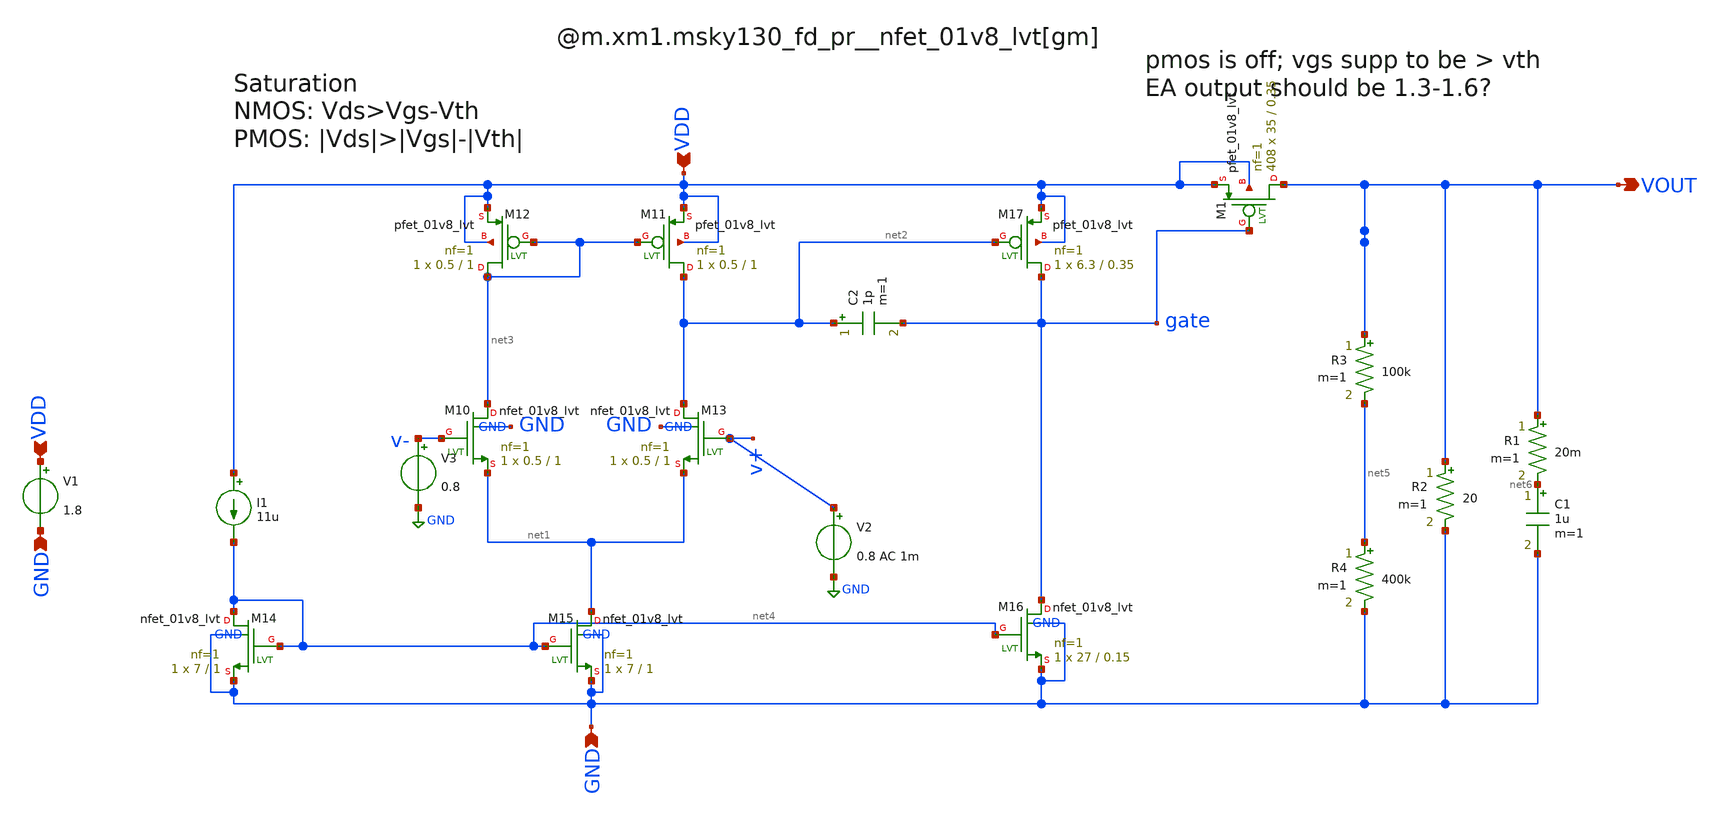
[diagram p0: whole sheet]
** sch_path: xschem/testbenches/FreqResponse-v2.sch
**.subckt FreqResponse-v2 VDD VOUT GND VDD GND
*.ipin VDD
*.opin VOUT
*.ipin GND
*.ipin VDD
*.ipin GND
C2 net2 gate 1p m=1
I1 VDD net4 11u
V3 v- GND 0.8
XM10 net3 v- net1 GND sky130_fd_pr__nfet_01v8_lvt L=1 W=0.5 nf=1 ad='int((1 + 1)/2) * 0.5 / 1 * 0.29'
+ as='int((1 + 2)/2) * 0.5 / 1 * 0.29' pd='2*int((1 + 1)/2) * (0.5 / 1 + 0.29)' ps='2*int((1 + 2)/2) * (0.5 / 1 + 0.29)'
+ nrd='0.29 / 0.5 ' nrs='0.29 / 0.5 ' sa=0 sb=0 sd=0 mult=1 m=1
XM11 net2 net3 VDD VDD sky130_fd_pr__pfet_01v8_lvt L=1 W=0.5 nf=1 ad='int((1 + 1)/2) * 0.5 / 1 * 0.29'
+ as='int((1 + 2)/2) * 0.5 / 1 * 0.29' pd='2*int((1 + 1)/2) * (0.5 / 1 + 0.29)' ps='2*int((1 + 2)/2) * (0.5 / 1 + 0.29)'
+ nrd='0.29 / 0.5 ' nrs='0.29 / 0.5 ' sa=0 sb=0 sd=0 mult=1 m=1
XM12 net3 net3 VDD VDD sky130_fd_pr__pfet_01v8_lvt L=1 W=0.5 nf=1 ad='int((1 + 1)/2) * 0.5 / 1 * 0.29'
+ as='int((1 + 2)/2) * 0.5 / 1 * 0.29' pd='2*int((1 + 1)/2) * (0.5 / 1 + 0.29)' ps='2*int((1 + 2)/2) * (0.5 / 1 + 0.29)'
+ nrd='0.29 / 0.5 ' nrs='0.29 / 0.5 ' sa=0 sb=0 sd=0 mult=1 m=1
XM13 net2 v+ net1 GND sky130_fd_pr__nfet_01v8_lvt L=1 W=0.5 nf=1 ad='int((1 + 1)/2) * 0.5 / 1 * 0.29'
+ as='int((1 + 2)/2) * 0.5 / 1 * 0.29' pd='2*int((1 + 1)/2) * (0.5 / 1 + 0.29)' ps='2*int((1 + 2)/2) * (0.5 / 1 + 0.29)'
+ nrd='0.29 / 0.5 ' nrs='0.29 / 0.5 ' sa=0 sb=0 sd=0 mult=1 m=1
XM14 net4 net4 GND GND sky130_fd_pr__nfet_01v8_lvt L=1 W=7 nf=1 ad='int((1 + 1)/2) * 7 / 1 * 0.29' as='int((1 + 2)/2) * 7 / 1 * 0.29'
+ pd='2*int((1 + 1)/2) * (7 / 1 + 0.29)' ps='2*int((1 + 2)/2) * (7 / 1 + 0.29)' nrd='0.29 / 7 ' nrs='0.29 / 7 '
+ sa=0 sb=0 sd=0 mult=1 m=1
XM15 net1 net4 GND GND sky130_fd_pr__nfet_01v8_lvt L=1 W=7 nf=1 ad='int((1 + 1)/2) * 7 / 1 * 0.29' as='int((1 + 2)/2) * 7 / 1 * 0.29'
+ pd='2*int((1 + 1)/2) * (7 / 1 + 0.29)' ps='2*int((1 + 2)/2) * (7 / 1 + 0.29)' nrd='0.29 / 7 ' nrs='0.29 / 7 '
+ sa=0 sb=0 sd=0 mult=1 m=1
XM16 gate net4 GND GND sky130_fd_pr__nfet_01v8_lvt L=0.15 W=27 nf=1 ad='int((1 + 1)/2) * 27 / 1 * 0.29'
+ as='int((1 + 2)/2) * 27 / 1 * 0.29' pd='2*int((1 + 1)/2) * (27 / 1 + 0.29)' ps='2*int((1 + 2)/2) * (27 / 1 + 0.29)'
+ nrd='0.29 / 27 ' nrs='0.29 / 27 ' sa=0 sb=0 sd=0 mult=1 m=1
XM17 gate net2 VDD VDD sky130_fd_pr__pfet_01v8_lvt L=0.35 W=6.3 nf=1 ad='int((1 + 1)/2) * 6.3 / 1 * 0.29'
+ as='int((1 + 2)/2) * 6.3 / 1 * 0.29' pd='2*int((1 + 1)/2) * (6.3 / 1 + 0.29)' ps='2*int((1 + 2)/2) * (6.3 / 1 + 0.29)'
+ nrd='0.29 / 6.3 ' nrs='0.29 / 6.3 ' sa=0 sb=0 sd=0 mult=1 m=1
R3 VOUT net5 100k m=1
R4 net5 GND 400k m=1
XM1 VOUT gate VDD VDD sky130_fd_pr__pfet_01v8_lvt L=0.35 W=35 nf=1 ad='int((1 + 1)/2) * 35 / 1 * 0.29'
+ as='int((1 + 2)/2) * 35 / 1 * 0.29' pd='2*int((1 + 1)/2) * (35 / 1 + 0.29)' ps='2*int((1 + 2)/2) * (35 / 1 + 0.29)'
+ nrd='0.29 / 35 ' nrs='0.29 / 35 ' sa=0 sb=0 sd=0 mult=408 m=408
V1 VDD GND 1.8
V2 v+ GND 0.8 AC 1m
R2 VOUT GND 20 m=1
C1 net6 GND 1u m=1
R1 VOUT net6 20m m=1
**** begin user architecture code



.lib /usr/local/share/pdk/sky130A/libs.tech/ngspice/sky130.lib.spice tt
.ac dec 20 1 1e12
*.tran 5u 5m

.control
run
print 1/@m.xm1.msky130_fd_pr__pfet_01v8_lvt[gds]
*plot vout
plot db(vout/v(v+)) title c=10p
plot 180*cph(vout)/pi
.endc


**** end user architecture code
**.ends
.GLOBAL GND
.end
